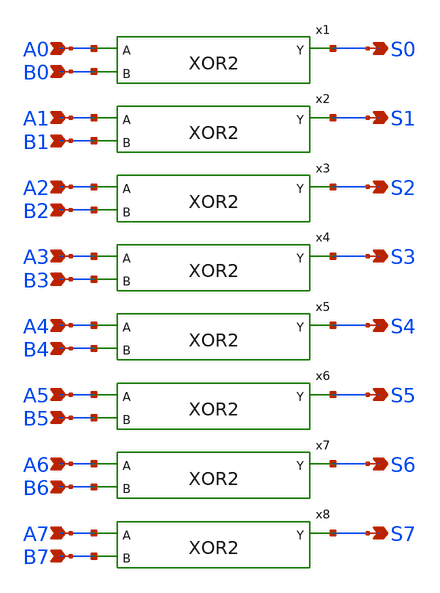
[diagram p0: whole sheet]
** sch_path: design/xschem/XOR/xor_8_bitwise.sch
**.subckt xor_8_bitwise S0 S1 S2 S3 S4 S5 S6 S7 A0 B0 A1 B1 A2 B2 A3 B3 A4 B4 A5 B5 A6 B6 A7 B7
*.opin S0
*.opin S1
*.opin S2
*.opin S3
*.opin S4
*.opin S5
*.opin S6
*.opin S7
*.ipin A0
*.ipin B0
*.ipin A1
*.ipin B1
*.ipin A2
*.ipin B2
*.ipin A3
*.ipin B3
*.ipin A4
*.ipin B4
*.ipin A5
*.ipin B5
*.ipin A6
*.ipin B6
*.ipin A7
*.ipin B7
x1 A0 B0 S0 VSS VDD XOR2
x2 A1 B1 S1 VSS VDD XOR2
x3 A2 B2 S2 VSS VDD XOR2
x4 A3 B3 S3 VSS VDD XOR2
x5 A4 B4 S4 VSS VDD XOR2
x6 A5 B5 S5 VSS VDD XOR2
x7 A6 B6 S6 VSS VDD XOR2
x8 A7 B7 S7 VSS VDD XOR2
**.ends
.end
